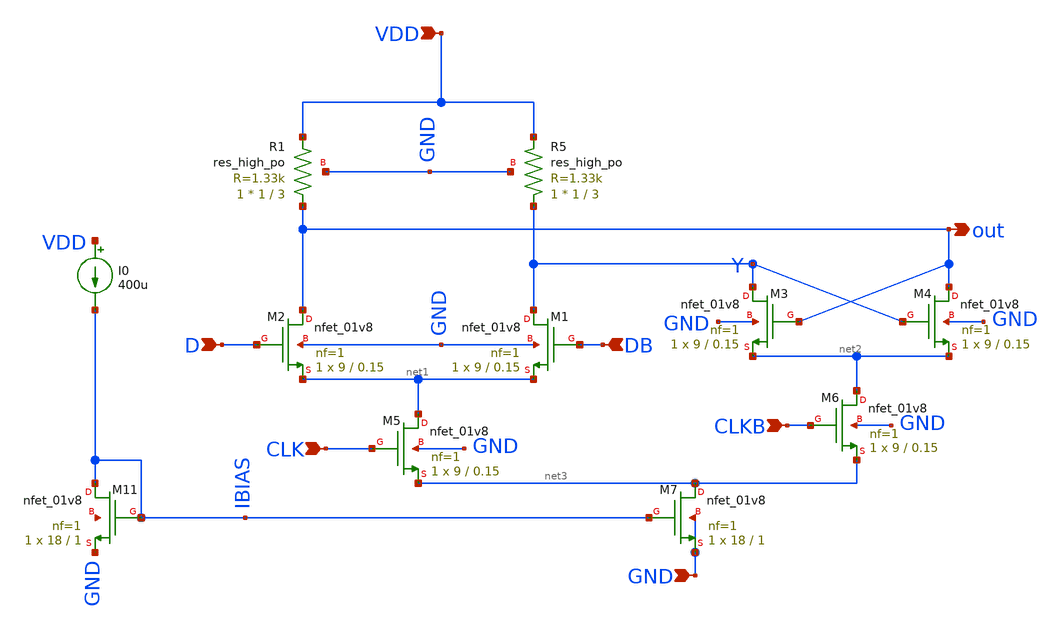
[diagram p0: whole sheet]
** sch_path: pll/dividers_lib/divider_design_trials/Testbench for testing latches/CML-latch.sch
**.subckt CML-latch GND VDD D DB CLK CLKB out
*.ipin GND
*.ipin VDD
*.ipin D
*.ipin DB
*.ipin CLK
*.ipin CLKB
*.opin out
XM2 out D net1 GND sky130_fd_pr__nfet_01v8 L=0.15 W=9 nf=1 ad='int((1 + 1)/2) * 9 / 1 * 0.29' as='int((1 + 2)/2) * 9 / 1 * 0.29'
+ pd='2*int((1 + 1)/2) * (9 / 1 + 0.29)' ps='2*int((1 + 2)/2) * (9 / 1 + 0.29)' nrd='0.29 / 9 ' nrs='0.29 / 9 '
+ sa=0 sb=0 sd=0 mult=1 m=1
XM1 Y DB net1 GND sky130_fd_pr__nfet_01v8 L=0.15 W=9 nf=1 ad='int((1 + 1)/2) * 9 / 1 * 0.29' as='int((1 + 2)/2) * 9 / 1 * 0.29'
+ pd='2*int((1 + 1)/2) * (9 / 1 + 0.29)' ps='2*int((1 + 2)/2) * (9 / 1 + 0.29)' nrd='0.29 / 9 ' nrs='0.29 / 9 '
+ sa=0 sb=0 sd=0 mult=1 m=1
XM3 Y out net2 GND sky130_fd_pr__nfet_01v8 L=0.15 W=9 nf=1 ad='int((1 + 1)/2) * 9 / 1 * 0.29' as='int((1 + 2)/2) * 9 / 1 * 0.29'
+ pd='2*int((1 + 1)/2) * (9 / 1 + 0.29)' ps='2*int((1 + 2)/2) * (9 / 1 + 0.29)' nrd='0.29 / 9 ' nrs='0.29 / 9 '
+ sa=0 sb=0 sd=0 mult=1 m=1
XM4 out Y net2 GND sky130_fd_pr__nfet_01v8 L=0.15 W=9 nf=1 ad='int((1 + 1)/2) * 9 / 1 * 0.29' as='int((1 + 2)/2) * 9 / 1 * 0.29'
+ pd='2*int((1 + 1)/2) * (9 / 1 + 0.29)' ps='2*int((1 + 2)/2) * (9 / 1 + 0.29)' nrd='0.29 / 9 ' nrs='0.29 / 9 '
+ sa=0 sb=0 sd=0 mult=1 m=1
XM5 net1 CLK net3 GND sky130_fd_pr__nfet_01v8 L=0.15 W=9 nf=1 ad='int((1 + 1)/2) * 9 / 1 * 0.29' as='int((1 + 2)/2) * 9 / 1 * 0.29'
+ pd='2*int((1 + 1)/2) * (9 / 1 + 0.29)' ps='2*int((1 + 2)/2) * (9 / 1 + 0.29)' nrd='0.29 / 9 ' nrs='0.29 / 9 '
+ sa=0 sb=0 sd=0 mult=1 m=1
XM6 net2 CLKB net3 GND sky130_fd_pr__nfet_01v8 L=0.15 W=9 nf=1 ad='int((1 + 1)/2) * 9 / 1 * 0.29' as='int((1 + 2)/2) * 9 / 1 * 0.29'
+ pd='2*int((1 + 1)/2) * (9 / 1 + 0.29)' ps='2*int((1 + 2)/2) * (9 / 1 + 0.29)' nrd='0.29 / 9 ' nrs='0.29 / 9 '
+ sa=0 sb=0 sd=0 mult=1 m=1
XM7 net3 IBIAS GND GND sky130_fd_pr__nfet_01v8 L=1 W=18 nf=1 ad='int((1 + 1)/2) * 18 / 1 * 0.29' as='int((1 + 2)/2) * 18 / 1 * 0.29'
+ pd='2*int((1 + 1)/2) * (18 / 1 + 0.29)' ps='2*int((1 + 2)/2) * (18 / 1 + 0.29)' nrd='0.29 / 18 ' nrs='0.29 / 18 '
+ sa=0 sb=0 sd=0 mult=1 m=1
I0 VDD IBIAS 400u
XM11 IBIAS IBIAS GND net4 sky130_fd_pr__nfet_01v8 L=1 W=18 nf=1 ad='int((1 + 1)/2) * 18 / 1 * 0.29' as='int((1 + 2)/2) * 18 / 1 * 0.29'
+ pd='2*int((1 + 1)/2) * (18 / 1 + 0.29)' ps='2*int((1 + 2)/2) * (18 / 1 + 0.29)' nrd='0.29 / 18 ' nrs='0.29 / 18 '
+ sa=0 sb=0 sd=0 mult=1 m=1
XR5 Y VDD GND sky130_fd_pr__res_high_po W=1 L=3 mult=1 m=1
XR1 out VDD GND sky130_fd_pr__res_high_po W=1 L=3 mult=1 m=1
**.ends
.end
